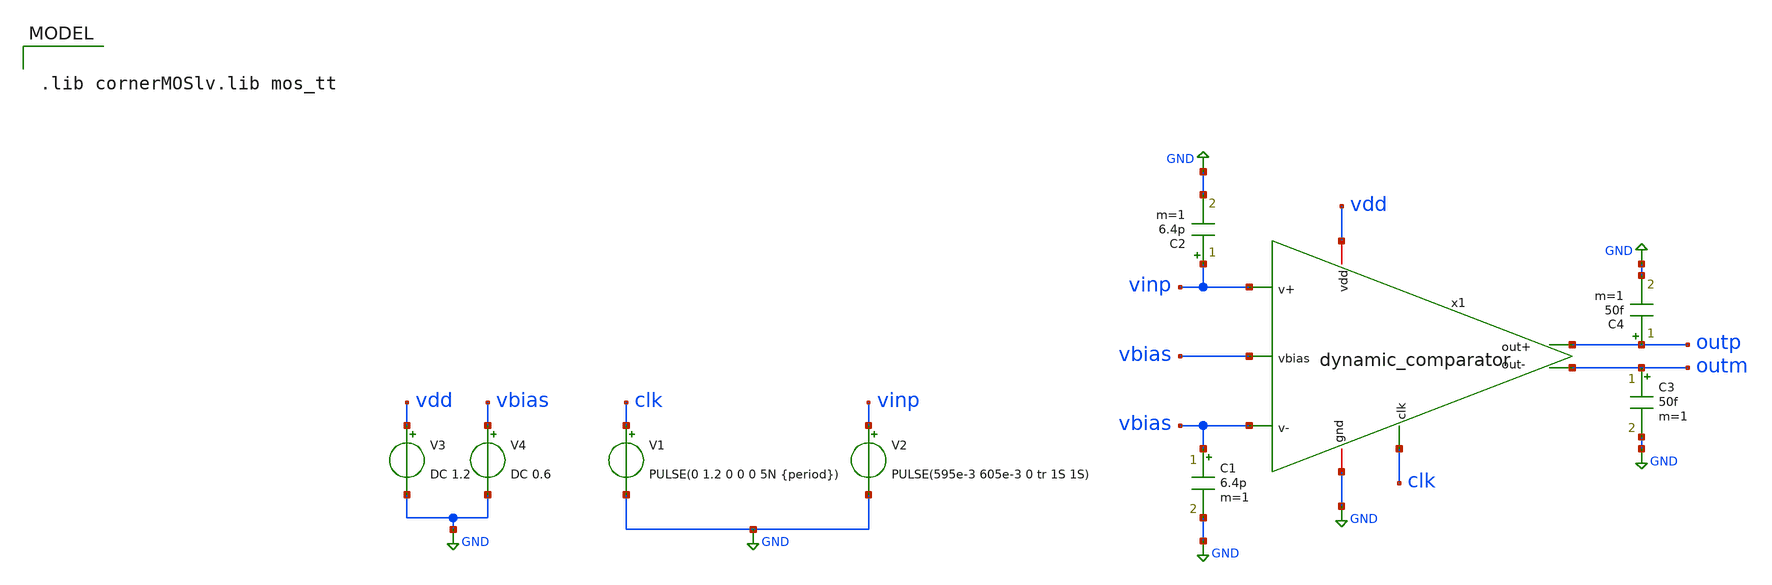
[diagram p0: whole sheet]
** sch_path: dependencies/ADC/ADC-main/schematic/xschem/comparator_tb.sch
**.subckt comparator_tb
V3 vdd GND DC 1.2
V4 vbias GND DC 0.6
V1 clk GND PULSE(0 1.2 0 0 0 5N {period})
V2 vinp GND PULSE(595e-3 605e-3 0 tr 1S 1S)
C1 vbias GND 6.4p m=1
C2 vinp GND 6.4p m=1
C4 outp GND 50f m=1
C3 outm GND 50f m=1
x1 vdd vbias vinp vbias outm outp clk GND dynamic_comparator
**** begin user architecture code

.lib cornerMOSlv.lib mos_tt



.param temp=27
.param clock = 100e6       ; 100 MHz clock
.param period = {1/clock}
.param num_cycles = 100
.param tr = {num_cycles * period}

.control
save all
* Operating point simulation
op
write comparator_tb.raw
set appendwrite

* Transient analysis
.options meas_step_max=1e-10
tran 500p 1u
let vindiff = v(vinp) - v(vbias)
let clk = v(clk)
let vout = v(outp) - v(outm)

meas TRAN rise_time TRIG v(outp) VAL=0.12  TD=9n RISE=4 TARG v(outp) VAL=1.08 TD=9n RISE=4
meas TRAN fall_time TRIG v(outp) VAL=1.08  TD=9n RISE=4 TARG v(outp) VAL=0.12 TD=9n RISE=4

write comparator_tb.raw
.endc


**** end user architecture code
**.ends
.GLOBAL GND
.end
